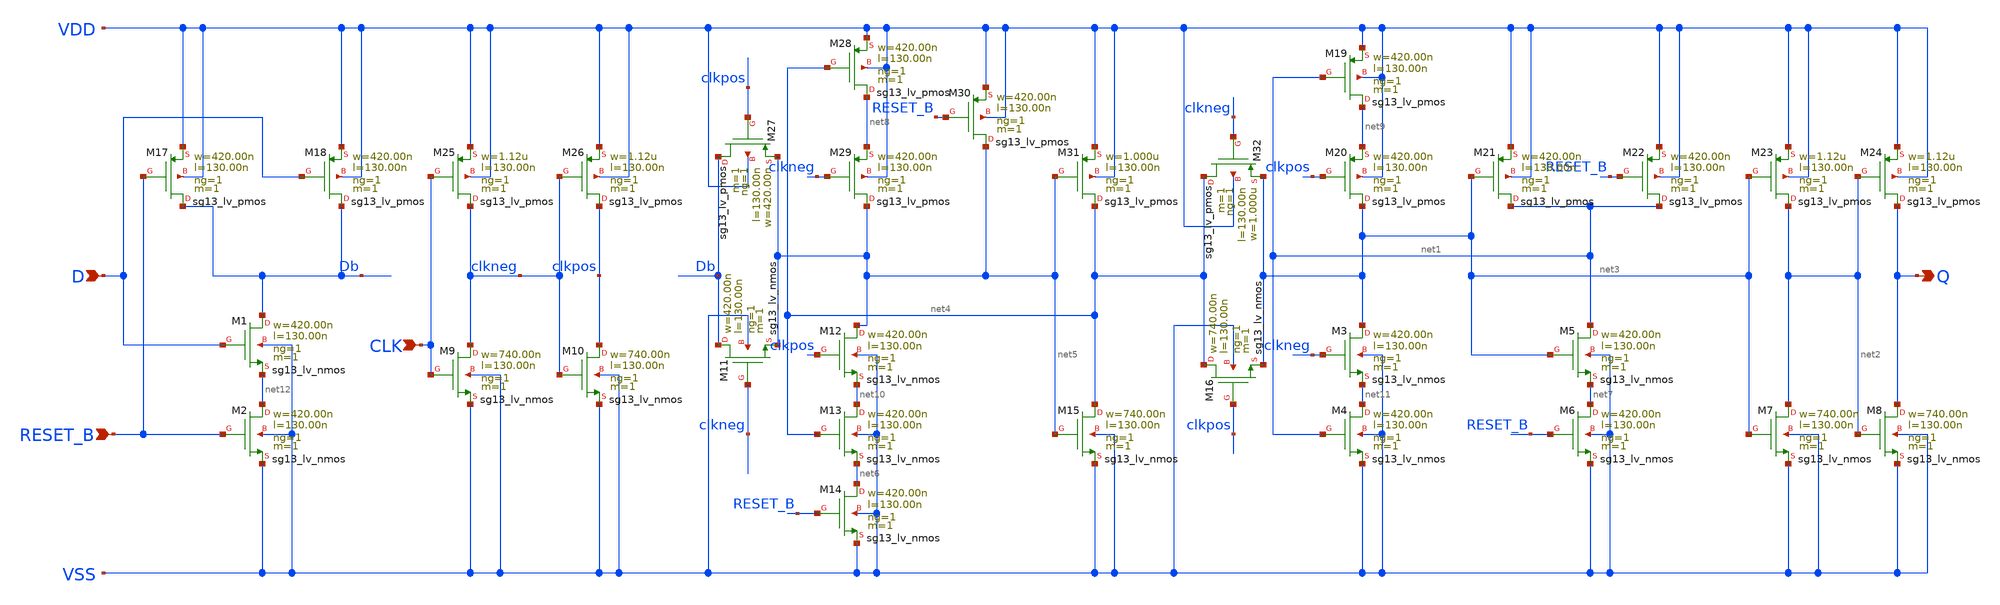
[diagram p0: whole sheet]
** sch_path: ihp-sg13g2/libs.tech/xschem/sg13g2_stdcells/sg13g2_dfrbpq_1.sch
**.subckt sg13g2_dfrbpq_1 Q CLK D RESET_B
*.opin Q
*.ipin CLK
*.ipin D
*.ipin RESET_B
XM1 Db D net12 VSS sg13_lv_nmos w=420.00n l=130.00n ng=1 m=1 mm_ok=1
XM2 net12 RESET_B VSS VSS sg13_lv_nmos w=420.00n l=130.00n ng=1 m=1 mm_ok=1
XM3 net3 clkneg net11 VSS sg13_lv_nmos w=420.00n l=130.00n ng=1 m=1 mm_ok=1
XM4 net11 net1 VSS VSS sg13_lv_nmos w=420.00n l=130.00n ng=1 m=1 mm_ok=1
XM5 net1 net3 net7 VSS sg13_lv_nmos w=420.00n l=130.00n ng=1 m=1 mm_ok=1
XM6 net7 RESET_B VSS VSS sg13_lv_nmos w=420.00n l=130.00n ng=1 m=1 mm_ok=1
XM7 net2 net3 VSS VSS sg13_lv_nmos w=740.00n l=130.00n ng=1 m=1 mm_ok=1
XM8 Q net2 VSS VSS sg13_lv_nmos w=740.00n l=130.00n ng=1 m=1 mm_ok=1
XM9 clkneg CLK VSS VSS sg13_lv_nmos w=740.00n l=130.00n ng=1 m=1 mm_ok=1
XM10 clkpos clkneg VSS VSS sg13_lv_nmos w=740.00n l=130.00n ng=1 m=1 mm_ok=1
XM11 Db clkneg net5 VSS sg13_lv_nmos w=420.00n l=130.00n ng=1 m=1 mm_ok=1
XM12 net5 clkpos net10 VSS sg13_lv_nmos w=420.00n l=130.00n ng=1 m=1 mm_ok=1
XM13 net10 net4 net6 VSS sg13_lv_nmos w=420.00n l=130.00n ng=1 m=1 mm_ok=1
XM14 net6 RESET_B VSS VSS sg13_lv_nmos w=420.00n l=130.00n ng=1 m=1 mm_ok=1
XM15 net4 net5 VSS VSS sg13_lv_nmos w=740.00n l=130.00n ng=1 m=1 mm_ok=1
XM16 net4 clkpos net3 VSS sg13_lv_nmos w=740.00n l=130.00n ng=1 m=1 mm_ok=1
XM17 Db RESET_B VDD VDD sg13_lv_pmos w=420.00n l=130.00n ng=1 m=1 mm_ok=1
XM18 Db D VDD VDD sg13_lv_pmos w=420.00n l=130.00n ng=1 m=1 mm_ok=1
XM19 net9 net1 VDD VDD sg13_lv_pmos w=420.00n l=130.00n ng=1 m=1 mm_ok=1
XM20 net3 clkpos net9 VDD sg13_lv_pmos w=420.00n l=130.00n ng=1 m=1 mm_ok=1
XM21 net1 net3 VDD VDD sg13_lv_pmos w=420.00n l=130.00n ng=1 m=1 mm_ok=1
XM22 net1 RESET_B VDD VDD sg13_lv_pmos w=420.00n l=130.00n ng=1 m=1 mm_ok=1
XM23 net2 net3 VDD VDD sg13_lv_pmos w=1.12u l=130.00n ng=1 m=1 mm_ok=1
XM24 Q net2 VDD VDD sg13_lv_pmos w=1.12u l=130.00n ng=1 m=1 mm_ok=1
XM25 clkneg CLK VDD VDD sg13_lv_pmos w=1.12u l=130.00n ng=1 m=1 mm_ok=1
XM26 clkpos clkneg VDD VDD sg13_lv_pmos w=1.12u l=130.00n ng=1 m=1 mm_ok=1
XM27 Db clkpos net5 VDD sg13_lv_pmos w=420.00n l=130.00n ng=1 m=1 mm_ok=1
XM28 net8 net4 VDD VDD sg13_lv_pmos w=420.00n l=130.00n ng=1 m=1 mm_ok=1
XM29 net5 clkneg net8 VDD sg13_lv_pmos w=420.00n l=130.00n ng=1 m=1 mm_ok=1
XM30 net5 RESET_B VDD VDD sg13_lv_pmos w=420.00n l=130.00n ng=1 m=1 mm_ok=1
XM31 net4 net5 VDD VDD sg13_lv_pmos w=1.000u l=130.00n ng=1 m=1 mm_ok=1
XM32 net4 clkneg net3 VDD sg13_lv_pmos w=1.000u l=130.00n ng=1 m=1 mm_ok=1
**.ends
.end
